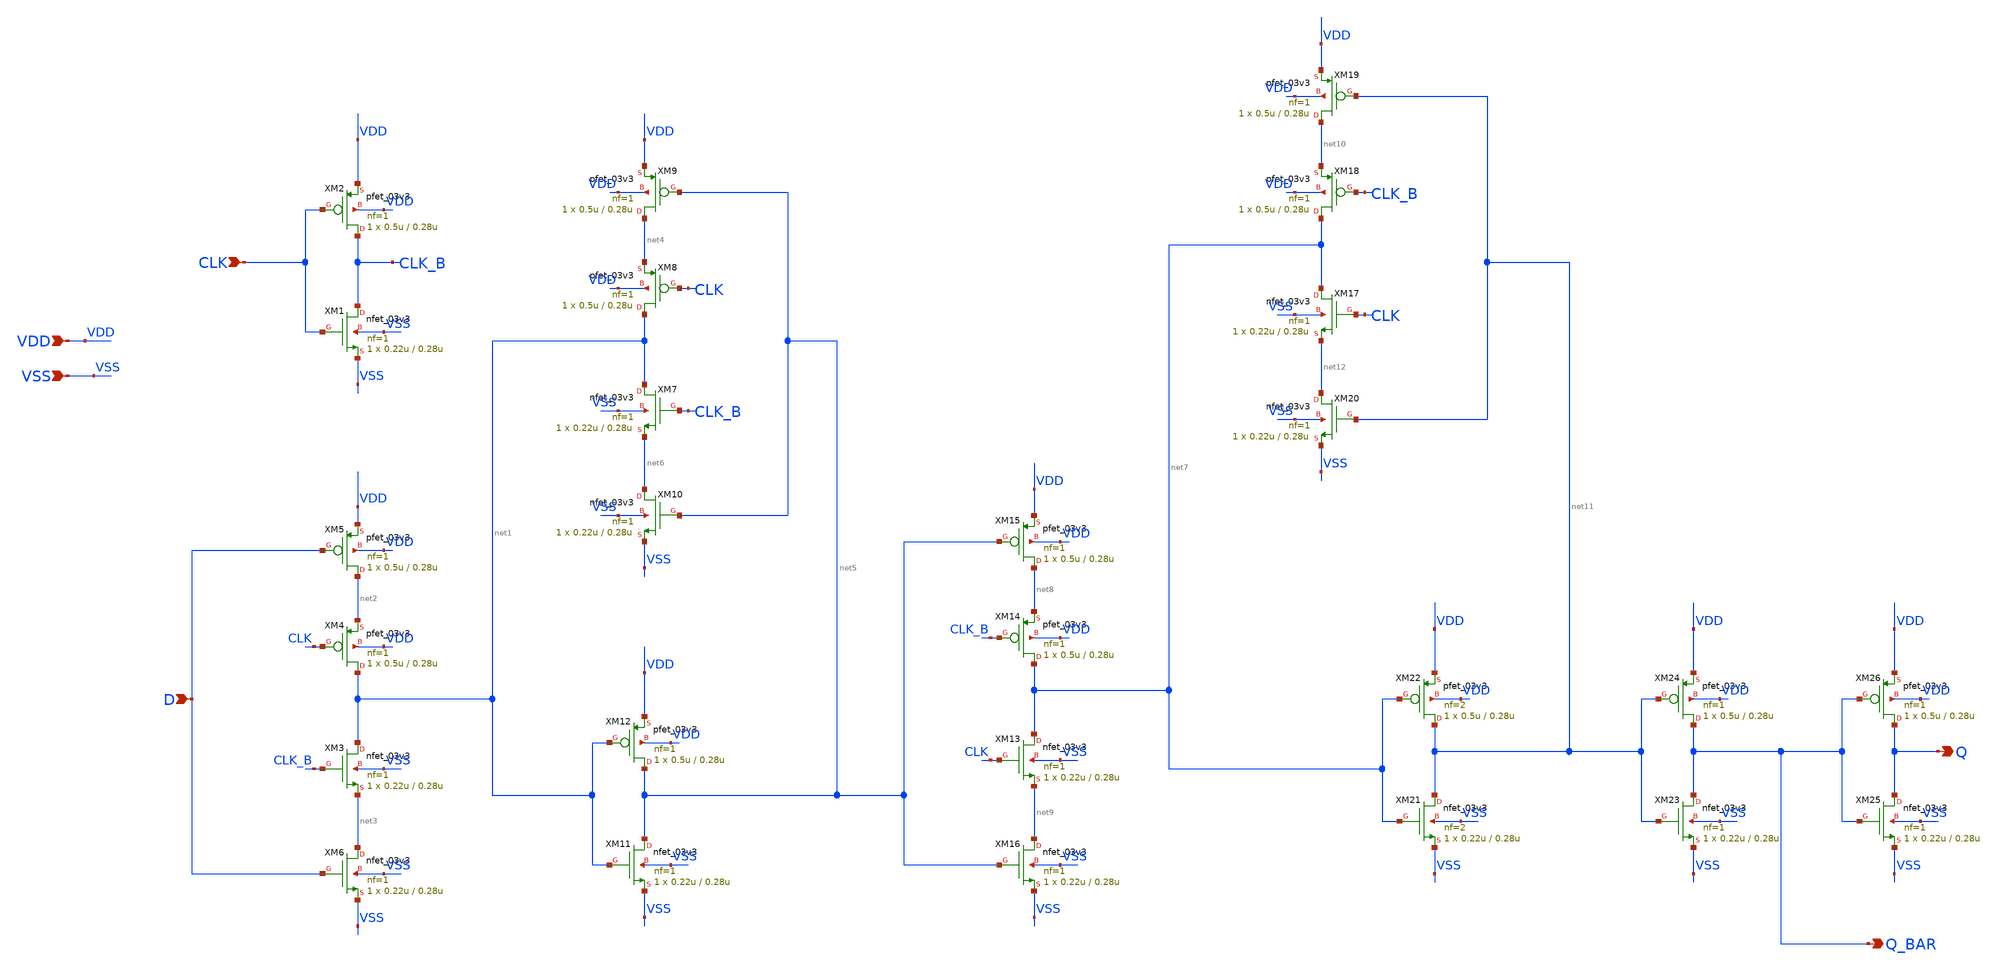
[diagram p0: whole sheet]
** sch_path: designs/libs/qw_core_analog_pkedit/DFF_3v3.sch
**.subckt DFF_3v3 CLK D Q_BAR VDD VSS Q
*.ipin CLK
*.ipin D
*.opin Q_BAR
*.ipin VDD
*.ipin VSS
*.opin Q
XM1 CLK_B CLK VSS VSS nfet_03v3 L=0.28u W=0.22u nf=1 ad='int((nf+1)/2) * W/nf * 0.18u' as='int((nf+2)/2) * W/nf * 0.18u'
+ pd='2*int((nf+1)/2) * (W/nf + 0.18u)' ps='2*int((nf+2)/2) * (W/nf + 0.18u)' nrd='0.18u / W' nrs='0.18u / W'
+ sa=0 sb=0 sd=0 m=1
XM2 CLK_B CLK VDD VDD pfet_03v3 L=0.28u W=0.5u nf=1 ad='int((nf+1)/2) * W/nf * 0.18u' as='int((nf+2)/2) * W/nf * 0.18u'
+ pd='2*int((nf+1)/2) * (W/nf + 0.18u)' ps='2*int((nf+2)/2) * (W/nf + 0.18u)' nrd='0.18u / W' nrs='0.18u / W'
+ sa=0 sb=0 sd=0 m=1
XM3 net1 CLK_B net3 VSS nfet_03v3 L=0.28u W=0.22u nf=1 ad='int((nf+1)/2) * W/nf * 0.18u' as='int((nf+2)/2) * W/nf * 0.18u'
+ pd='2*int((nf+1)/2) * (W/nf + 0.18u)' ps='2*int((nf+2)/2) * (W/nf + 0.18u)' nrd='0.18u / W' nrs='0.18u / W'
+ sa=0 sb=0 sd=0 m=1
XM4 net1 CLK net2 VDD pfet_03v3 L=0.28u W=0.5u nf=1 ad='int((nf+1)/2) * W/nf * 0.18u' as='int((nf+2)/2) * W/nf * 0.18u'
+ pd='2*int((nf+1)/2) * (W/nf + 0.18u)' ps='2*int((nf+2)/2) * (W/nf + 0.18u)' nrd='0.18u / W' nrs='0.18u / W'
+ sa=0 sb=0 sd=0 m=1
XM5 net2 D VDD VDD pfet_03v3 L=0.28u W=0.5u nf=1 ad='int((nf+1)/2) * W/nf * 0.18u' as='int((nf+2)/2) * W/nf * 0.18u'
+ pd='2*int((nf+1)/2) * (W/nf + 0.18u)' ps='2*int((nf+2)/2) * (W/nf + 0.18u)' nrd='0.18u / W' nrs='0.18u / W'
+ sa=0 sb=0 sd=0 m=1
XM6 net3 D VSS VSS nfet_03v3 L=0.28u W=0.22u nf=1 ad='int((nf+1)/2) * W/nf * 0.18u' as='int((nf+2)/2) * W/nf * 0.18u'
+ pd='2*int((nf+1)/2) * (W/nf + 0.18u)' ps='2*int((nf+2)/2) * (W/nf + 0.18u)' nrd='0.18u / W' nrs='0.18u / W'
+ sa=0 sb=0 sd=0 m=1
XM7 net1 CLK_B net6 VSS nfet_03v3 L=0.28u W=0.22u nf=1 ad='int((nf+1)/2) * W/nf * 0.18u' as='int((nf+2)/2) * W/nf * 0.18u'
+ pd='2*int((nf+1)/2) * (W/nf + 0.18u)' ps='2*int((nf+2)/2) * (W/nf + 0.18u)' nrd='0.18u / W' nrs='0.18u / W'
+ sa=0 sb=0 sd=0 m=1
XM8 net1 CLK net4 VDD pfet_03v3 L=0.28u W=0.5u nf=1 ad='int((nf+1)/2) * W/nf * 0.18u' as='int((nf+2)/2) * W/nf * 0.18u'
+ pd='2*int((nf+1)/2) * (W/nf + 0.18u)' ps='2*int((nf+2)/2) * (W/nf + 0.18u)' nrd='0.18u / W' nrs='0.18u / W'
+ sa=0 sb=0 sd=0 m=1
XM9 net4 net5 VDD VDD pfet_03v3 L=0.28u W=0.5u nf=1 ad='int((nf+1)/2) * W/nf * 0.18u' as='int((nf+2)/2) * W/nf * 0.18u'
+ pd='2*int((nf+1)/2) * (W/nf + 0.18u)' ps='2*int((nf+2)/2) * (W/nf + 0.18u)' nrd='0.18u / W' nrs='0.18u / W'
+ sa=0 sb=0 sd=0 m=1
XM10 net6 net5 VSS VSS nfet_03v3 L=0.28u W=0.22u nf=1 ad='int((nf+1)/2) * W/nf * 0.18u' as='int((nf+2)/2) * W/nf * 0.18u'
+ pd='2*int((nf+1)/2) * (W/nf + 0.18u)' ps='2*int((nf+2)/2) * (W/nf + 0.18u)' nrd='0.18u / W' nrs='0.18u / W'
+ sa=0 sb=0 sd=0 m=1
XM11 net5 net1 VSS VSS nfet_03v3 L=0.28u W=0.22u nf=1 ad='int((nf+1)/2) * W/nf * 0.18u' as='int((nf+2)/2) * W/nf * 0.18u'
+ pd='2*int((nf+1)/2) * (W/nf + 0.18u)' ps='2*int((nf+2)/2) * (W/nf + 0.18u)' nrd='0.18u / W' nrs='0.18u / W'
+ sa=0 sb=0 sd=0 m=1
XM12 net5 net1 VDD VDD pfet_03v3 L=0.28u W=0.5u nf=1 ad='int((nf+1)/2) * W/nf * 0.18u' as='int((nf+2)/2) * W/nf * 0.18u'
+ pd='2*int((nf+1)/2) * (W/nf + 0.18u)' ps='2*int((nf+2)/2) * (W/nf + 0.18u)' nrd='0.18u / W' nrs='0.18u / W'
+ sa=0 sb=0 sd=0 m=1
XM13 net7 CLK net9 VSS nfet_03v3 L=0.28u W=0.22u nf=1 ad='int((nf+1)/2) * W/nf * 0.18u' as='int((nf+2)/2) * W/nf * 0.18u'
+ pd='2*int((nf+1)/2) * (W/nf + 0.18u)' ps='2*int((nf+2)/2) * (W/nf + 0.18u)' nrd='0.18u / W' nrs='0.18u / W'
+ sa=0 sb=0 sd=0 m=1
XM14 net7 CLK_B net8 VDD pfet_03v3 L=0.28u W=0.5u nf=1 ad='int((nf+1)/2) * W/nf * 0.18u' as='int((nf+2)/2) * W/nf * 0.18u'
+ pd='2*int((nf+1)/2) * (W/nf + 0.18u)' ps='2*int((nf+2)/2) * (W/nf + 0.18u)' nrd='0.18u / W' nrs='0.18u / W'
+ sa=0 sb=0 sd=0 m=1
XM15 net8 net5 VDD VDD pfet_03v3 L=0.28u W=0.5u nf=1 ad='int((nf+1)/2) * W/nf * 0.18u' as='int((nf+2)/2) * W/nf * 0.18u'
+ pd='2*int((nf+1)/2) * (W/nf + 0.18u)' ps='2*int((nf+2)/2) * (W/nf + 0.18u)' nrd='0.18u / W' nrs='0.18u / W'
+ sa=0 sb=0 sd=0 m=1
XM16 net9 net5 VSS VSS nfet_03v3 L=0.28u W=0.22u nf=1 ad='int((nf+1)/2) * W/nf * 0.18u' as='int((nf+2)/2) * W/nf * 0.18u'
+ pd='2*int((nf+1)/2) * (W/nf + 0.18u)' ps='2*int((nf+2)/2) * (W/nf + 0.18u)' nrd='0.18u / W' nrs='0.18u / W'
+ sa=0 sb=0 sd=0 m=1
XM17 net7 CLK net12 VSS nfet_03v3 L=0.28u W=0.22u nf=1 ad='int((nf+1)/2) * W/nf * 0.18u' as='int((nf+2)/2) * W/nf * 0.18u'
+ pd='2*int((nf+1)/2) * (W/nf + 0.18u)' ps='2*int((nf+2)/2) * (W/nf + 0.18u)' nrd='0.18u / W' nrs='0.18u / W'
+ sa=0 sb=0 sd=0 m=1
XM18 net7 CLK_B net10 VDD pfet_03v3 L=0.28u W=0.5u nf=1 ad='int((nf+1)/2) * W/nf * 0.18u' as='int((nf+2)/2) * W/nf * 0.18u'
+ pd='2*int((nf+1)/2) * (W/nf + 0.18u)' ps='2*int((nf+2)/2) * (W/nf + 0.18u)' nrd='0.18u / W' nrs='0.18u / W'
+ sa=0 sb=0 sd=0 m=1
XM19 net10 net11 VDD VDD pfet_03v3 L=0.28u W=0.5u nf=1 ad='int((nf+1)/2) * W/nf * 0.18u' as='int((nf+2)/2) * W/nf * 0.18u'
+ pd='2*int((nf+1)/2) * (W/nf + 0.18u)' ps='2*int((nf+2)/2) * (W/nf + 0.18u)' nrd='0.18u / W' nrs='0.18u / W'
+ sa=0 sb=0 sd=0 m=1
XM20 net12 net11 VSS VSS nfet_03v3 L=0.28u W=0.22u nf=1 ad='int((nf+1)/2) * W/nf * 0.18u' as='int((nf+2)/2) * W/nf * 0.18u'
+ pd='2*int((nf+1)/2) * (W/nf + 0.18u)' ps='2*int((nf+2)/2) * (W/nf + 0.18u)' nrd='0.18u / W' nrs='0.18u / W'
+ sa=0 sb=0 sd=0 m=1
XM21 net11 net7 VSS VSS nfet_03v3 L=0.28u W=0.22u nf=2 ad='int((nf+1)/2) * W/nf * 0.18u' as='int((nf+2)/2) * W/nf * 0.18u'
+ pd='2*int((nf+1)/2) * (W/nf + 0.18u)' ps='2*int((nf+2)/2) * (W/nf + 0.18u)' nrd='0.18u / W' nrs='0.18u / W'
+ sa=0 sb=0 sd=0 m=1
XM22 net11 net7 VDD VDD pfet_03v3 L=0.28u W=0.5u nf=2 ad='int((nf+1)/2) * W/nf * 0.18u' as='int((nf+2)/2) * W/nf * 0.18u'
+ pd='2*int((nf+1)/2) * (W/nf + 0.18u)' ps='2*int((nf+2)/2) * (W/nf + 0.18u)' nrd='0.18u / W' nrs='0.18u / W'
+ sa=0 sb=0 sd=0 m=1
XM23 Q_BAR net11 VSS VSS nfet_03v3 L=0.28u W=0.22u nf=1 ad='int((nf+1)/2) * W/nf * 0.18u' as='int((nf+2)/2) * W/nf * 0.18u'
+ pd='2*int((nf+1)/2) * (W/nf + 0.18u)' ps='2*int((nf+2)/2) * (W/nf + 0.18u)' nrd='0.18u / W' nrs='0.18u / W'
+ sa=0 sb=0 sd=0 m=1
XM24 Q_BAR net11 VDD VDD pfet_03v3 L=0.28u W=0.5u nf=1 ad='int((nf+1)/2) * W/nf * 0.18u' as='int((nf+2)/2) * W/nf * 0.18u'
+ pd='2*int((nf+1)/2) * (W/nf + 0.18u)' ps='2*int((nf+2)/2) * (W/nf + 0.18u)' nrd='0.18u / W' nrs='0.18u / W'
+ sa=0 sb=0 sd=0 m=1
XM25 Q Q_BAR VSS VSS nfet_03v3 L=0.28u W=0.22u nf=1 ad='int((nf+1)/2) * W/nf * 0.18u' as='int((nf+2)/2) * W/nf * 0.18u'
+ pd='2*int((nf+1)/2) * (W/nf + 0.18u)' ps='2*int((nf+2)/2) * (W/nf + 0.18u)' nrd='0.18u / W' nrs='0.18u / W'
+ sa=0 sb=0 sd=0 m=1
XM26 Q Q_BAR VDD VDD pfet_03v3 L=0.28u W=0.5u nf=1 ad='int((nf+1)/2) * W/nf * 0.18u' as='int((nf+2)/2) * W/nf * 0.18u'
+ pd='2*int((nf+1)/2) * (W/nf + 0.18u)' ps='2*int((nf+2)/2) * (W/nf + 0.18u)' nrd='0.18u / W' nrs='0.18u / W'
+ sa=0 sb=0 sd=0 m=1
**.ends
.end
